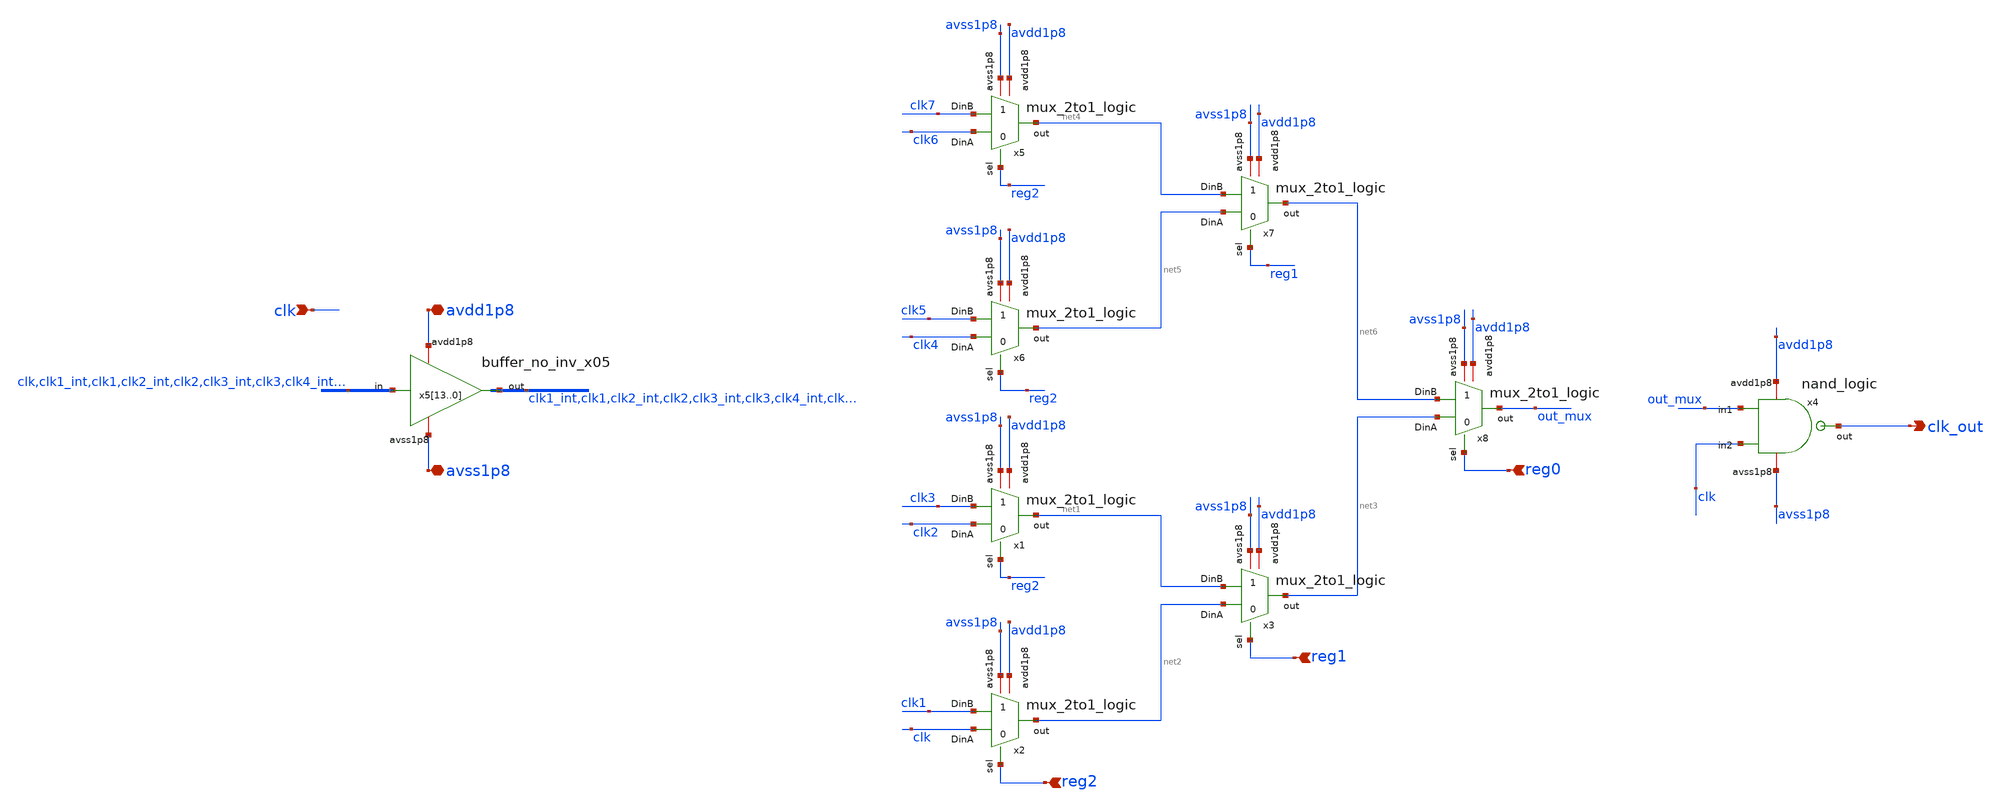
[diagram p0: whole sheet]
** sch_path: xschem/afernandez_residue_amplifier/delay_cell_buff.sch
**.subckt delay_cell_buff clk avdd1p8 avss1p8 clk_out reg2 reg1 reg0
*.ipin clk
*.iopin avdd1p8
*.iopin avss1p8
*.opin clk_out
*.ipin reg2
*.ipin reg1
*.ipin reg0
x1 avdd1p8 reg2 avss1p8 clk3 net1 clk2 mux_2to1_logic
x2 avdd1p8 reg2 avss1p8 clk1 net2 clk mux_2to1_logic
x3 avdd1p8 reg1 avss1p8 net1 net3 net2 mux_2to1_logic
x4 avdd1p8 out_mux clk_out clk avss1p8 nand_logic
x513 avdd1p8 clk avss1p8 clk1_int buffer_no_inv_x05
x512 avdd1p8 clk1_int avss1p8 clk1 buffer_no_inv_x05
x511 avdd1p8 clk1 avss1p8 clk2_int buffer_no_inv_x05
x510 avdd1p8 clk2_int avss1p8 clk2 buffer_no_inv_x05
x59 avdd1p8 clk2 avss1p8 clk3_int buffer_no_inv_x05
x58 avdd1p8 clk3_int avss1p8 clk3 buffer_no_inv_x05
x57 avdd1p8 clk3 avss1p8 clk4_int buffer_no_inv_x05
x56 avdd1p8 clk4_int avss1p8 clk4 buffer_no_inv_x05
x55 avdd1p8 clk4 avss1p8 clk5_int buffer_no_inv_x05
x54 avdd1p8 clk5_int avss1p8 clk5 buffer_no_inv_x05
x53 avdd1p8 clk5 avss1p8 clk6_int buffer_no_inv_x05
x52 avdd1p8 clk6_int avss1p8 clk6 buffer_no_inv_x05
x51 avdd1p8 clk6 avss1p8 clk7_int buffer_no_inv_x05
x50 avdd1p8 clk7_int avss1p8 clk7 buffer_no_inv_x05
x5 avdd1p8 reg2 avss1p8 clk7 net4 clk6 mux_2to1_logic
x6 avdd1p8 reg2 avss1p8 clk5 net5 clk4 mux_2to1_logic
x7 avdd1p8 reg1 avss1p8 net4 net6 net5 mux_2to1_logic
x8 avdd1p8 reg0 avss1p8 net6 out_mux net3 mux_2to1_logic
**.ends
.end
